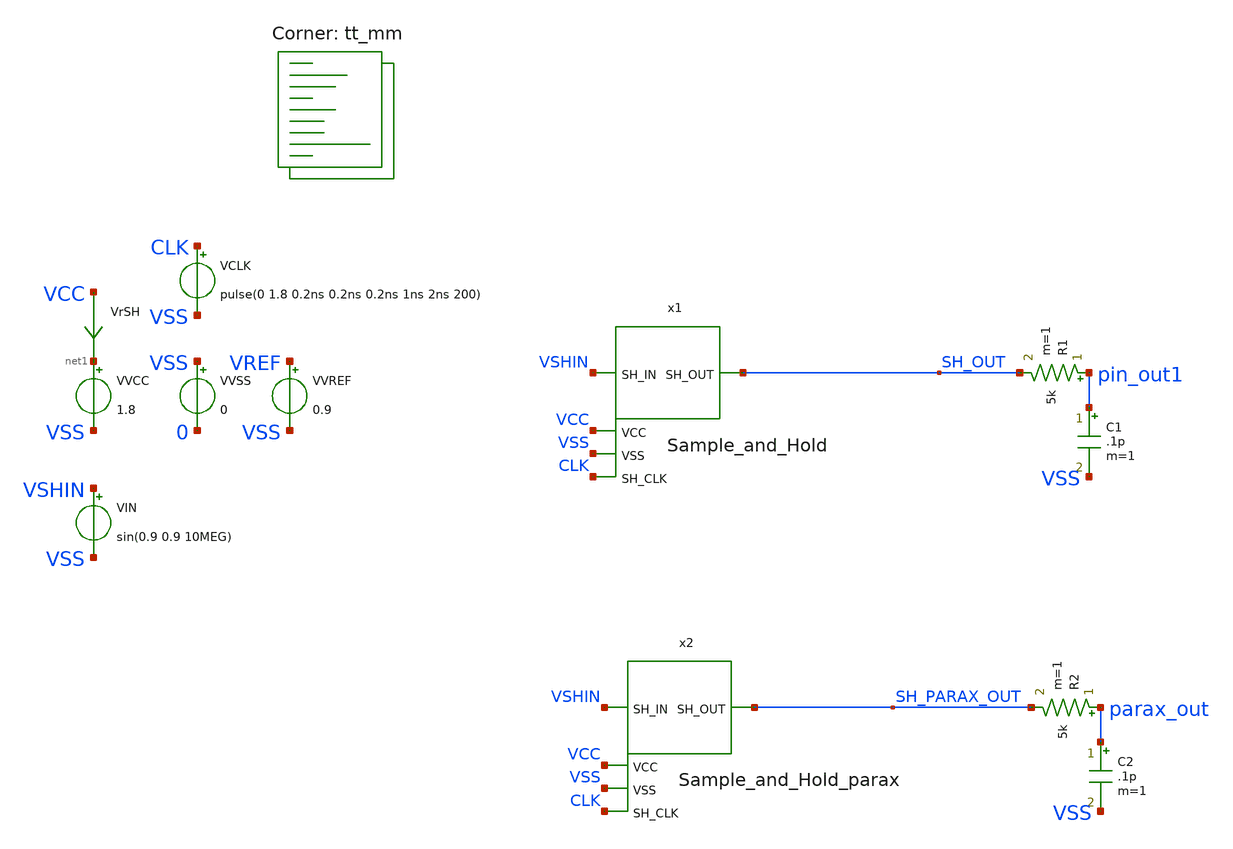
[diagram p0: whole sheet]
** sch_path: xschem/testbench.sch
**.subckt testbench
x1 SH_OUT VSHIN VSS VCC CLK Sample_and_Hold
VCLK CLK VSS pulse(0 1.8 0.2ns 0.2ns 0.2ns 1ns 2ns 200)
VVCC net1 VSS 1.8
VVSS VSS 0 0
VIN VSHIN VSS sin(0.9 0.9 10MEG)
VVREF VREF VSS 0.9
R1 pin_out1 SH_OUT 5k m=1
C1 pin_out1 VSS .1p m=1
VrSH VCC net1 0
.save i(vrsh)
x2 SH_PARAX_OUT VSHIN VSS VCC CLK Sample_and_Hold_parax
R2 parax_out SH_PARAX_OUT 5k m=1
C2 parax_out VSS .1p m=1
**** begin user architecture code
.lib $::SKYWATER_MODELS/sky130.lib.spice tt_mm


.option chgtol=4e-16 method=gear
.param VCC = 1.8
.param VREF = 0.9
.param temp = 25
*vvcc VCC 0 1.8
*vvss VSS 0 0
*vvref VREF 0 0.9
*vclk CLK pulse(1ns 1ns 1ns 5ns 10ns 25)
*vvshin VSHIN sin(0.9 0.9 10MEG)


.control
  save all
  savecurrents
  op
  write testbench.raw
  reset
  set appendwrite
  *repeat 5
    save all
    tran 0.1n 250n uic
    write testbench.raw
    set appendwrite
    reset
  *end
  quit 0
.endc

**** end user architecture code
**.ends

* expanding   symbol:  Sample_and_Hold.sym # of pins=5
** sym_path: xschem/Sample_and_Hold.sym
** sch_path: xschem/Sample_and_Hold.sch
.subckt Sample_and_Hold SH_OUT SH_IN VSS VCC SH_CLK
*.ipin SH_IN
*.ipin SH_CLK
*.opin SH_OUT
*.ipin VSS
*.ipin VCC
XC1 SH_OUT VSS sky130_fd_pr__cap_mim_m3_1 W=2 L=2 MF=5 m=5
XM6 SH_OUT CLKN SH_IN VCC sky130_fd_pr__pfet_01v8 L=0.15 W=2 nf=2 ad='int((nf+1)/2) * W/nf * 0.29' as='int((nf+2)/2) * W/nf * 0.29'
+ pd='2*int((nf+1)/2) * (W/nf + 0.29)' ps='2*int((nf+2)/2) * (W/nf + 0.29)' nrd='0.29 / W' nrs='0.29 / W'
+ sa=0 sb=0 sd=0 mult=1 m=1
XM7 SH_IN CLKB SH_OUT VSS sky130_fd_pr__nfet_01v8 L=0.15 W=1 nf=1 ad='int((nf+1)/2) * W/nf * 0.29' as='int((nf+2)/2) * W/nf * 0.29'
+ pd='2*int((nf+1)/2) * (W/nf + 0.29)' ps='2*int((nf+2)/2) * (W/nf + 0.29)' nrd='0.29 / W' nrs='0.29 / W'
+ sa=0 sb=0 sd=0 mult=1 m=1
XM8 CLKN SH_CLK VSS VSS sky130_fd_pr__nfet_01v8 L=0.15 W=1 nf=1 ad='int((nf+1)/2) * W/nf * 0.29' as='int((nf+2)/2) * W/nf * 0.29'
+ pd='2*int((nf+1)/2) * (W/nf + 0.29)' ps='2*int((nf+2)/2) * (W/nf + 0.29)' nrd='0.29 / W' nrs='0.29 / W'
+ sa=0 sb=0 sd=0 mult=1 m=1
XM9 CLKN SH_CLK VCC VCC sky130_fd_pr__pfet_01v8 L=0.15 W=2 nf=2 ad='int((nf+1)/2) * W/nf * 0.29' as='int((nf+2)/2) * W/nf * 0.29'
+ pd='2*int((nf+1)/2) * (W/nf + 0.29)' ps='2*int((nf+2)/2) * (W/nf + 0.29)' nrd='0.29 / W' nrs='0.29 / W'
+ sa=0 sb=0 sd=0 mult=1 m=1
XM10 CLKB CLKN VSS VSS sky130_fd_pr__nfet_01v8 L=0.15 W=1 nf=1 ad='int((nf+1)/2) * W/nf * 0.29' as='int((nf+2)/2) * W/nf * 0.29'
+ pd='2*int((nf+1)/2) * (W/nf + 0.29)' ps='2*int((nf+2)/2) * (W/nf + 0.29)' nrd='0.29 / W' nrs='0.29 / W'
+ sa=0 sb=0 sd=0 mult=1 m=1
XM1 CLKB CLKN VCC VCC sky130_fd_pr__pfet_01v8 L=0.15 W=2 nf=2 ad='int((nf+1)/2) * W/nf * 0.29' as='int((nf+2)/2) * W/nf * 0.29'
+ pd='2*int((nf+1)/2) * (W/nf + 0.29)' ps='2*int((nf+2)/2) * (W/nf + 0.29)' nrd='0.29 / W' nrs='0.29 / W'
+ sa=0 sb=0 sd=0 mult=1 m=1
.ends


* expanding   symbol:  Sample_and_Hold_parax.sym # of pins=5
** sym_path: xschem/Sample_and_Hold.sym
.include [file normalize ../mag/Sample_and_Hold.sim.spice]
.end
